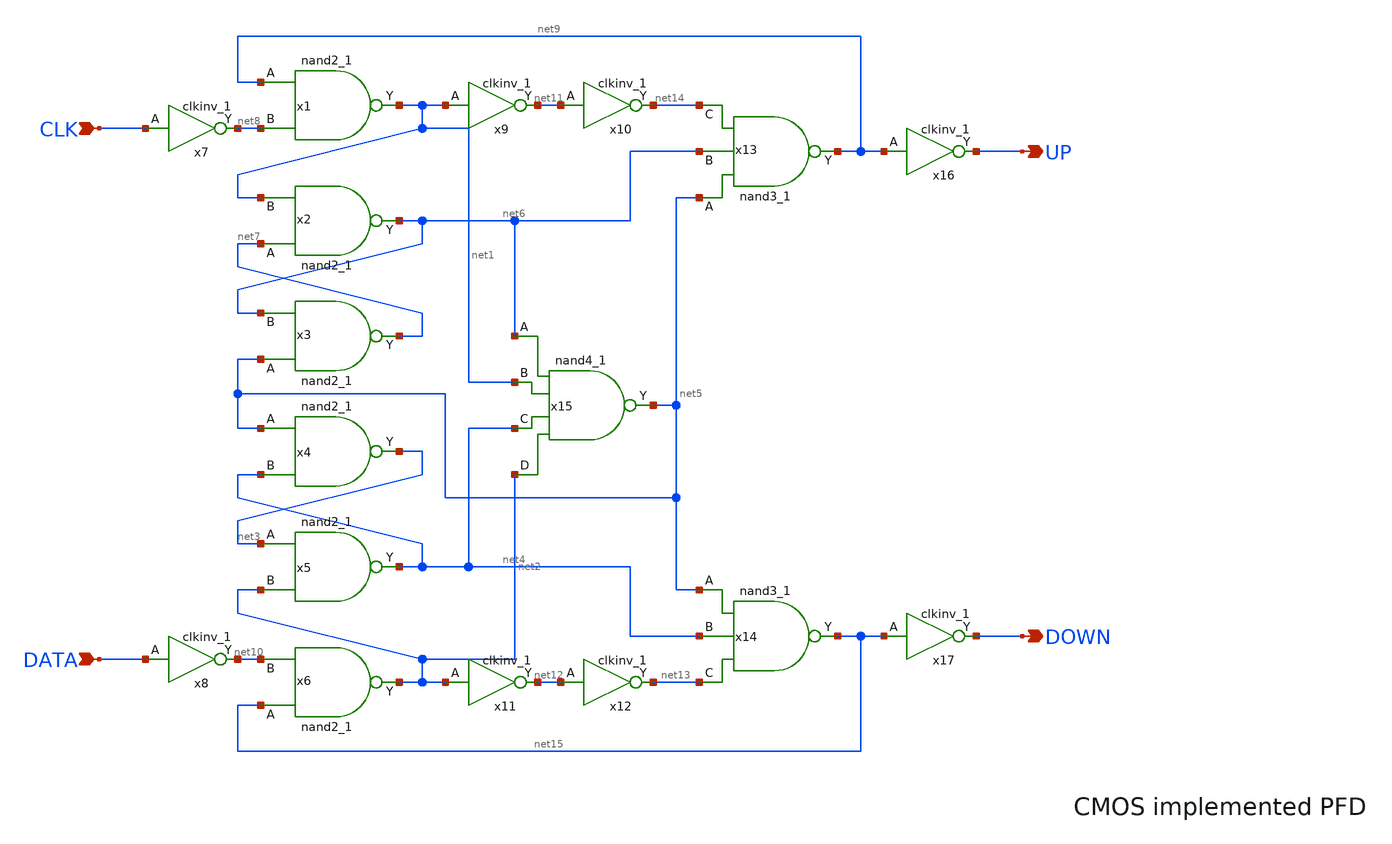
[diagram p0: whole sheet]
** sch_path: pfd2.sch
**.subckt pfd2 DATA CLK UP DOWN
*.ipin DATA
*.ipin CLK
*.opin UP
*.opin DOWN
x1 net9 net8 VGND VNB VPB VPWR net1 gf180mcu_fd_sc_mcu7t5v0__nand2_1
x7 CLK VGND VNB VPB VPWR net8 gf180mcu_fd_sc_mcu7t5v0__clkinv_1
x2 net7 net1 VGND VNB VPB VPWR net6 gf180mcu_fd_sc_mcu7t5v0__nand2_1
x3 net5 net6 VGND VNB VPB VPWR net7 gf180mcu_fd_sc_mcu7t5v0__nand2_1
x4 net5 net4 VGND VNB VPB VPWR net3 gf180mcu_fd_sc_mcu7t5v0__nand2_1
x5 net3 net2 VGND VNB VPB VPWR net4 gf180mcu_fd_sc_mcu7t5v0__nand2_1
x6 net15 net10 VGND VNB VPB VPWR net2 gf180mcu_fd_sc_mcu7t5v0__nand2_1
x8 DATA VGND VNB VPB VPWR net10 gf180mcu_fd_sc_mcu7t5v0__clkinv_1
x13 net5 net6 net14 VGND VNB VPB VPWR net9 gf180mcu_fd_sc_mcu7t5v0__nand3_1
x14 net5 net4 net13 VGND VNB VPB VPWR net15 gf180mcu_fd_sc_mcu7t5v0__nand3_1
x15 net6 net1 net4 net2 VGND VNB VPB VPWR net5 gf180mcu_fd_sc_mcu7t5v0__nand4_1
x9 net1 VGND VNB VPB VPWR net11 gf180mcu_fd_sc_mcu7t5v0__clkinv_1
x10 net11 VGND VNB VPB VPWR net14 gf180mcu_fd_sc_mcu7t5v0__clkinv_1
x11 net2 VGND VNB VPB VPWR net12 gf180mcu_fd_sc_mcu7t5v0__clkinv_1
x12 net12 VGND VNB VPB VPWR net13 gf180mcu_fd_sc_mcu7t5v0__clkinv_1
x16 net9 VGND VNB VPB VPWR UP gf180mcu_fd_sc_mcu7t5v0__clkinv_1
x17 net15 VGND VNB VPB VPWR DOWN gf180mcu_fd_sc_mcu7t5v0__clkinv_1
**.ends
.end
